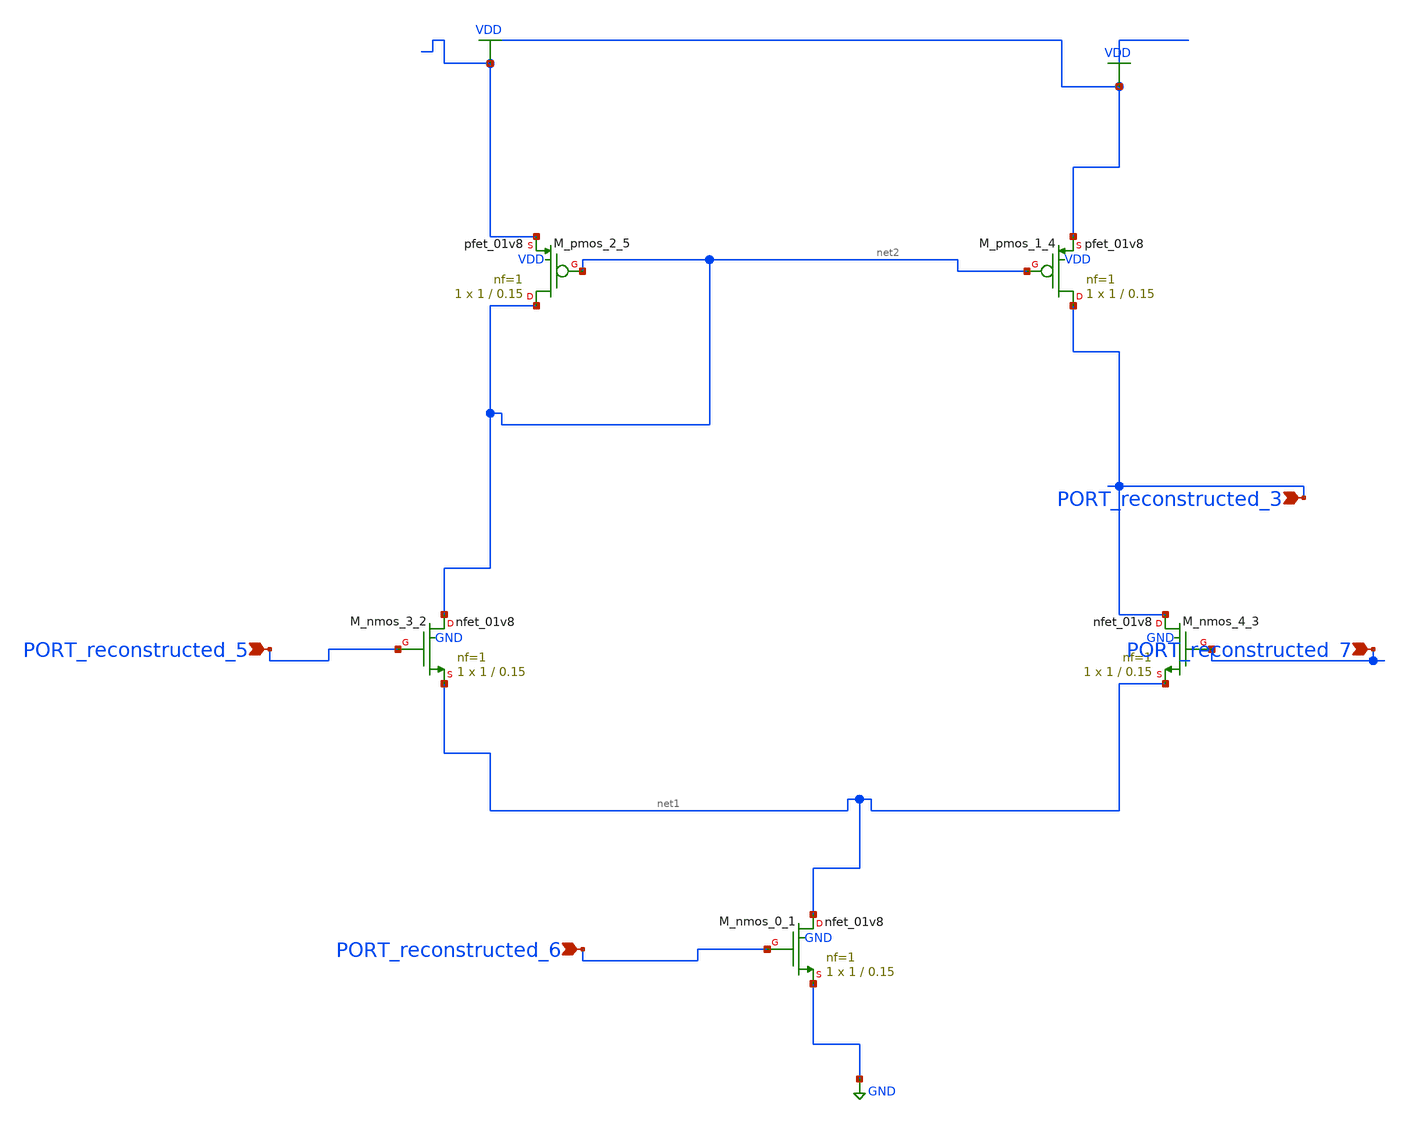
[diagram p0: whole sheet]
** sch_path: schematics/AMSNet/276.sch
**.subckt 276 PORT_reconstructed_5 PORT_reconstructed_6 PORT_reconstructed_7 PORT_reconstructed_3
*.ipin PORT_reconstructed_5
*.ipin PORT_reconstructed_6
*.ipin PORT_reconstructed_7
*.ipin PORT_reconstructed_3
XM_nmos_0_1 net1 PORT_reconstructed_6 GND GND sky130_fd_pr__nfet_01v8 L=0.15 W=1 nf=1 ad='int((1 + 1)/2) * 1 / 1 * 0.29'
+ as='int((1 + 2)/2) * 1 / 1 * 0.29' pd='2*int((1 + 1)/2) * (1 / 1 + 0.29)' ps='2*int((1 + 2)/2) * (1 / 1 + 0.29)'
+ nrd='0.29 / 1 ' nrs='0.29 / 1 ' sa=0 sb=0 sd=0 mult=1 m=1
XM_nmos_3_2 net2 PORT_reconstructed_5 net1 GND sky130_fd_pr__nfet_01v8 L=0.15 W=1 nf=1 ad='int((1 + 1)/2) * 1 / 1 * 0.29'
+ as='int((1 + 2)/2) * 1 / 1 * 0.29' pd='2*int((1 + 1)/2) * (1 / 1 + 0.29)' ps='2*int((1 + 2)/2) * (1 / 1 + 0.29)'
+ nrd='0.29 / 1 ' nrs='0.29 / 1 ' sa=0 sb=0 sd=0 mult=1 m=1
XM_nmos_4_3 PORT_reconstructed_3 PORT_reconstructed_7 net1 GND sky130_fd_pr__nfet_01v8 L=0.15 W=1 nf=1
+ ad='int((1 + 1)/2) * 1 / 1 * 0.29' as='int((1 + 2)/2) * 1 / 1 * 0.29' pd='2*int((1 + 1)/2) * (1 / 1 + 0.29)'
+ ps='2*int((1 + 2)/2) * (1 / 1 + 0.29)' nrd='0.29 / 1 ' nrs='0.29 / 1 ' sa=0 sb=0 sd=0 mult=1 m=1
XM_pmos_1_4 PORT_reconstructed_3 net2 VDD VDD sky130_fd_pr__pfet_01v8 L=0.15 W=1 nf=1 ad='int((1 + 1)/2) * 1 / 1 * 0.29'
+ as='int((1 + 2)/2) * 1 / 1 * 0.29' pd='2*int((1 + 1)/2) * (1 / 1 + 0.29)' ps='2*int((1 + 2)/2) * (1 / 1 + 0.29)'
+ nrd='0.29 / 1 ' nrs='0.29 / 1 ' sa=0 sb=0 sd=0 mult=1 m=1
XM_pmos_2_5 net2 net2 VDD VDD sky130_fd_pr__pfet_01v8 L=0.15 W=1 nf=1 ad='int((1 + 1)/2) * 1 / 1 * 0.29'
+ as='int((1 + 2)/2) * 1 / 1 * 0.29' pd='2*int((1 + 1)/2) * (1 / 1 + 0.29)' ps='2*int((1 + 2)/2) * (1 / 1 + 0.29)'
+ nrd='0.29 / 1 ' nrs='0.29 / 1 ' sa=0 sb=0 sd=0 mult=1 m=1
**.ends
.GLOBAL GND
.GLOBAL VDD
.end
